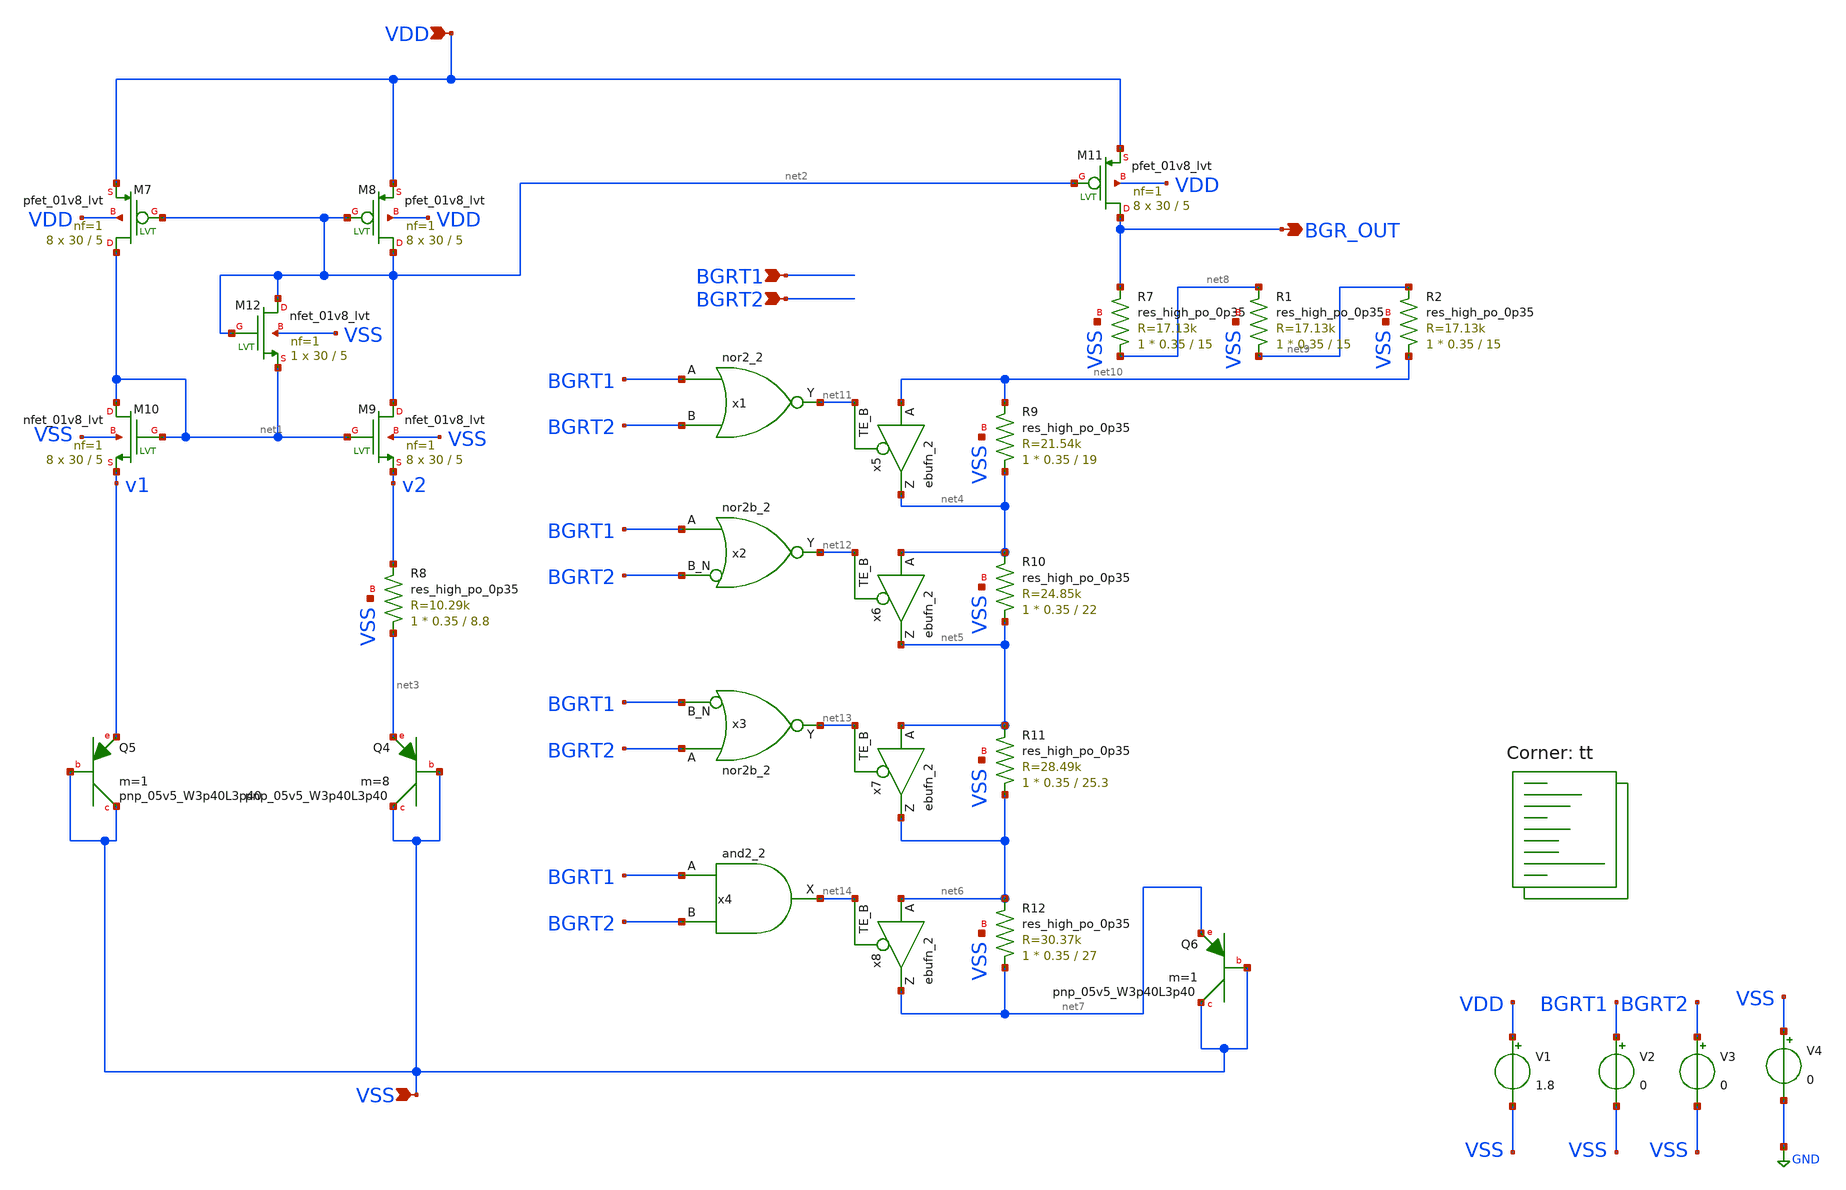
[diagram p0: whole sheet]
** sch_path: xschem/bandgap.sch
**.subckt bandgap BGR_OUT VDD VSS BGRT1 BGRT2
*.opin BGR_OUT
*.ipin VDD
*.ipin VSS
*.ipin BGRT1
*.ipin BGRT2
XM7 net1 net2 VDD VDD sky130_fd_pr__pfet_01v8_lvt L=5 W=30 nf=1 ad='int((nf+1)/2) * W/nf * 0.29' as='int((nf+2)/2) * W/nf * 0.29'
+ pd='2*int((nf+1)/2) * (W/nf + 0.29)' ps='2*int((nf+2)/2) * (W/nf + 0.29)' nrd='0.29 / W' nrs='0.29 / W'
+ sa=0 sb=0 sd=0 mult=8 m=8
XM8 net2 net2 VDD VDD sky130_fd_pr__pfet_01v8_lvt L=5 W=30 nf=1 ad='int((nf+1)/2) * W/nf * 0.29' as='int((nf+2)/2) * W/nf * 0.29'
+ pd='2*int((nf+1)/2) * (W/nf + 0.29)' ps='2*int((nf+2)/2) * (W/nf + 0.29)' nrd='0.29 / W' nrs='0.29 / W'
+ sa=0 sb=0 sd=0 mult=8 m=8
XM9 net2 net1 v2 VSS sky130_fd_pr__nfet_01v8_lvt L=5 W=30 nf=1 ad='int((nf+1)/2) * W/nf * 0.29' as='int((nf+2)/2) * W/nf * 0.29'
+ pd='2*int((nf+1)/2) * (W/nf + 0.29)' ps='2*int((nf+2)/2) * (W/nf + 0.29)' nrd='0.29 / W' nrs='0.29 / W'
+ sa=0 sb=0 sd=0 mult=8 m=8
XM10 net1 net1 v1 VSS sky130_fd_pr__nfet_01v8_lvt L=5 W=30 nf=1 ad='int((nf+1)/2) * W/nf * 0.29' as='int((nf+2)/2) * W/nf * 0.29'
+ pd='2*int((nf+1)/2) * (W/nf + 0.29)' ps='2*int((nf+2)/2) * (W/nf + 0.29)' nrd='0.29 / W' nrs='0.29 / W'
+ sa=0 sb=0 sd=0 mult=8 m=8
XQ4 VSS VSS net3 sky130_fd_pr__pnp_05v5_W3p40L3p40 m=8
XQ5 VSS VSS v1 sky130_fd_pr__pnp_05v5_W3p40L3p40 m=1
XM11 BGR_OUT net2 VDD VDD sky130_fd_pr__pfet_01v8_lvt L=5 W=30 nf=1 ad='int((nf+1)/2) * W/nf * 0.29'
+ as='int((nf+2)/2) * W/nf * 0.29' pd='2*int((nf+1)/2) * (W/nf + 0.29)' ps='2*int((nf+2)/2) * (W/nf + 0.29)'
+ nrd='0.29 / W' nrs='0.29 / W' sa=0 sb=0 sd=0 mult=8 m=8
XM12 net2 net2 net1 VSS sky130_fd_pr__nfet_01v8_lvt L=5 W=30 nf=1 ad='int((nf+1)/2) * W/nf * 0.29' as='int((nf+2)/2) * W/nf * 0.29'
+ pd='2*int((nf+1)/2) * (W/nf + 0.29)' ps='2*int((nf+2)/2) * (W/nf + 0.29)' nrd='0.29 / W' nrs='0.29 / W'
+ sa=0 sb=0 sd=0 mult=1 m=1
XQ6 VSS VSS net7 sky130_fd_pr__pnp_05v5_W3p40L3p40 m=1
V1 VDD VSS 1.8
V2 BGRT1 VSS 0
V3 BGRT2 VSS 0
x5 net10 net11 VSS VSS VDD VDD net4 sky130_fd_sc_hd__ebufn_2
x6 net4 net12 VSS VSS VDD VDD net5 sky130_fd_sc_hd__ebufn_2
x7 net5 net13 VSS VSS VDD VDD net6 sky130_fd_sc_hd__ebufn_2
x8 net6 net14 VSS VSS VDD VDD net7 sky130_fd_sc_hd__ebufn_2
V4 VSS GND 0
x1 BGRT1 BGRT2 VSS VSS VDD VDD net11 sky130_fd_sc_hd__nor2_2
x2 BGRT1 BGRT2 VSS VSS VDD VDD net12 sky130_fd_sc_hd__nor2b_2
x3 BGRT2 BGRT1 VSS VSS VDD VDD net13 sky130_fd_sc_hd__nor2b_2
x4 BGRT1 BGRT2 VSS VSS VDD VDD net14 sky130_fd_sc_hd__and2_2
XR7 net8 BGR_OUT VSS sky130_fd_pr__res_high_po_0p35 L=15 mult=1 m=1
XR1 net9 net8 VSS sky130_fd_pr__res_high_po_0p35 L=15 mult=1 m=1
XR2 net10 net9 VSS sky130_fd_pr__res_high_po_0p35 L=15 mult=1 m=1
XR9 net4 net10 VSS sky130_fd_pr__res_high_po_0p35 L=19 mult=1 m=1
XR10 net5 net4 VSS sky130_fd_pr__res_high_po_0p35 L=22 mult=1 m=1
XR11 net6 net5 VSS sky130_fd_pr__res_high_po_0p35 L=25.3 mult=1 m=1
XR12 net7 net6 VSS sky130_fd_pr__res_high_po_0p35 L=27 mult=1 m=1
XR8 net3 v2 VSS sky130_fd_pr__res_high_po_0p35 L=8.8 mult=1 m=1
**** begin user architecture code

.include /foss/pdks/sky130A/libs.ref/sky130_fd_sc_hd/spice/sky130_fd_sc_hd.spice
.saveall
.dc temp -40 120


.lib $::SKYWATER_MODELS/sky130.lib.spice tt
**** end user architecture code
**.ends
.GLOBAL GND
.end
